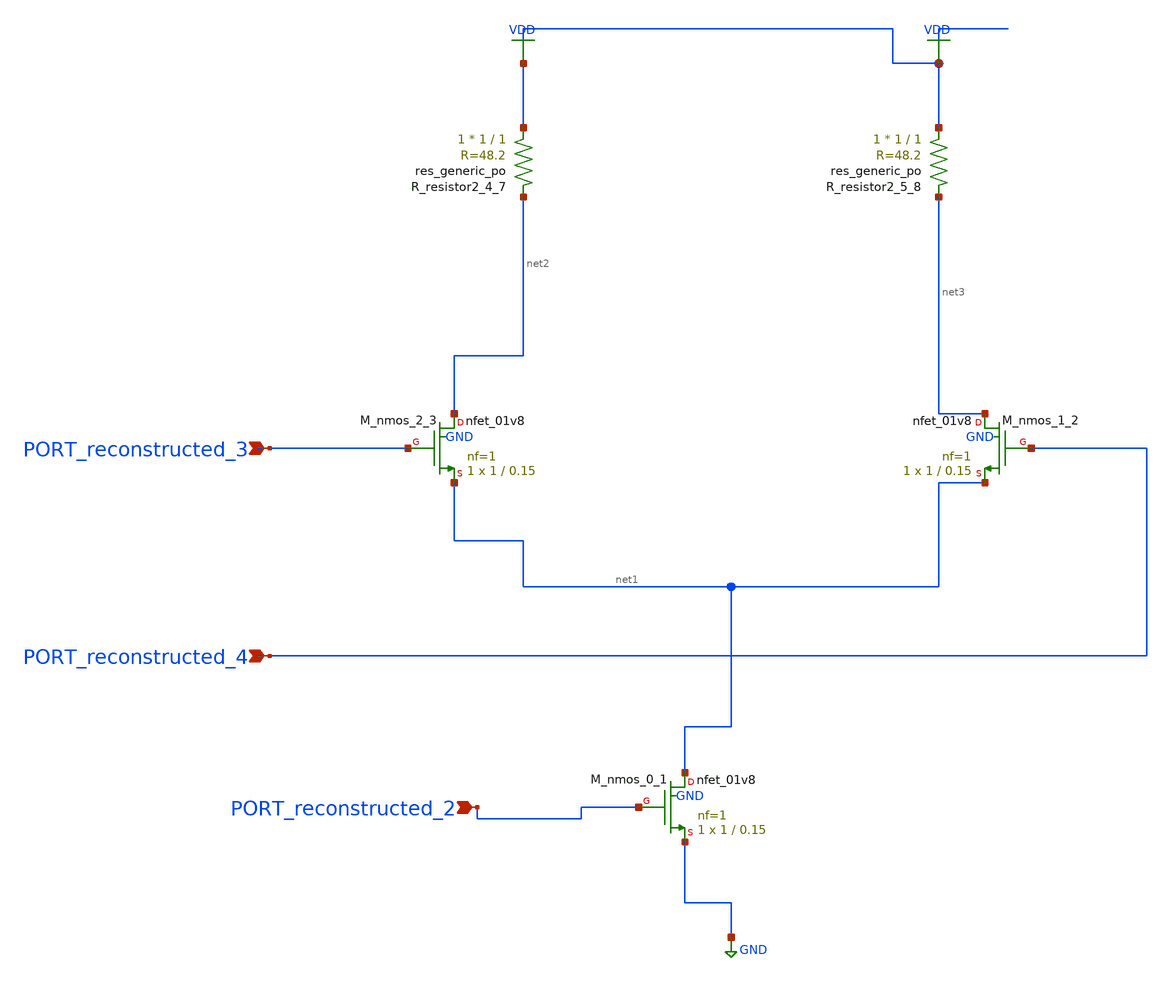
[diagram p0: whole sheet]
** sch_path: schematics/AMSNet/192.sch
**.subckt 192 PORT_reconstructed_2 PORT_reconstructed_3 PORT_reconstructed_4
*.ipin PORT_reconstructed_2
*.ipin PORT_reconstructed_3
*.ipin PORT_reconstructed_4
XM_nmos_0_1 net1 PORT_reconstructed_2 GND GND sky130_fd_pr__nfet_01v8 L=0.15 W=1 nf=1 ad='int((1 + 1)/2) * 1 / 1 * 0.29'
+ as='int((1 + 2)/2) * 1 / 1 * 0.29' pd='2*int((1 + 1)/2) * (1 / 1 + 0.29)' ps='2*int((1 + 2)/2) * (1 / 1 + 0.29)'
+ nrd='0.29 / 1 ' nrs='0.29 / 1 ' sa=0 sb=0 sd=0 mult=1 m=1
XM_nmos_1_2 net3 PORT_reconstructed_4 net1 GND sky130_fd_pr__nfet_01v8 L=0.15 W=1 nf=1 ad='int((1 + 1)/2) * 1 / 1 * 0.29'
+ as='int((1 + 2)/2) * 1 / 1 * 0.29' pd='2*int((1 + 1)/2) * (1 / 1 + 0.29)' ps='2*int((1 + 2)/2) * (1 / 1 + 0.29)'
+ nrd='0.29 / 1 ' nrs='0.29 / 1 ' sa=0 sb=0 sd=0 mult=1 m=1
XM_nmos_2_3 net2 PORT_reconstructed_3 net1 GND sky130_fd_pr__nfet_01v8 L=0.15 W=1 nf=1 ad='int((1 + 1)/2) * 1 / 1 * 0.29'
+ as='int((1 + 2)/2) * 1 / 1 * 0.29' pd='2*int((1 + 1)/2) * (1 / 1 + 0.29)' ps='2*int((1 + 2)/2) * (1 / 1 + 0.29)'
+ nrd='0.29 / 1 ' nrs='0.29 / 1 ' sa=0 sb=0 sd=0 mult=1 m=1
XR_resistor2_4_7 VDD net2 sky130_fd_pr__res_generic_po W=1 L=1 m=1
XR_resistor2_5_8 VDD net3 sky130_fd_pr__res_generic_po W=1 L=1 m=1
**.ends
.GLOBAL GND
.GLOBAL VDD
.end
